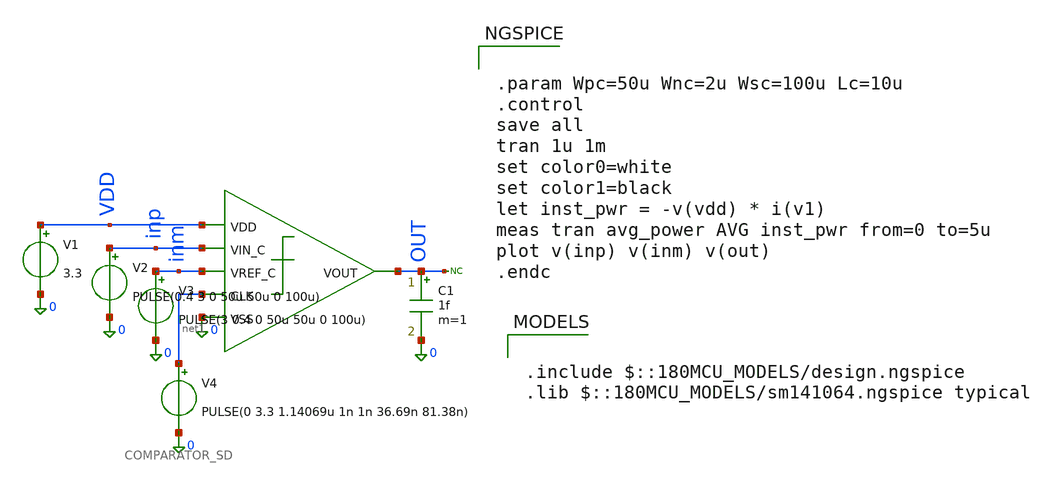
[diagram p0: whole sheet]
** sch_path: src/schematics/latched_comparator/COMP_TB.sch
**.subckt COMP_TB
* noconn OUT
V2 inp 0 PULSE(0.4 3 0 50u 50u 0 100u)
V4 net1 0 PULSE(0 3.3 1.14069u 1n 1n 36.69n 81.38n)
V1 VDD 0 3.3
C1 OUT 0 1f m=1
x1 VDD inp inm net1 OUT 0 COMPARATOR_SD
V3 inm 0 PULSE(3 0.4 0 50u 50u 0 100u)
**** begin user architecture code


.param Wpc=50u Wnc=2u Wsc=100u Lc=10u
.control
save all
tran 1u 1m
set color0=white
set color1=black
let inst_pwr = -v(vdd) * i(v1)
meas tran avg_power AVG inst_pwr from=0 to=5u
plot v(inp) v(inm) v(out)
.endc




.include $::180MCU_MODELS/design.ngspice
.lib $::180MCU_MODELS/sm141064.ngspice typical

**** end user architecture code
**.ends

* expanding   symbol:
*+  /foss/designs/low-power-12b-first-order-delta-sigma-adc/src/schematics/latched_comparator/COMPARATOR_SD.sym # of pins=6
** sym_path: /foss/designs/low-power-12b-first-order-delta-sigma-adc/src/schematics/latched_comparator/COMPARATOR_SD.sym
** sch_path: /foss/designs/low-power-12b-first-order-delta-sigma-adc/src/schematics/latched_comparator/COMPARATOR_SD.sch
.subckt COMPARATOR_SD VDD VIN_C VREF_C CLK VOUT VSS
*.ipin VIN_C
*.ipin VREF_C
*.ipin CLK
*.opin VOUT
*.ipin VDD
*.ipin VSS
XM1 net3 VIN_C net1 VDD pfet_03v3 L=Lc W=Wpc nf=1 ad='int((nf+1)/2) * W/nf * 0.18u' as='int((nf+2)/2) * W/nf * 0.18u'
+ pd='2*int((nf+1)/2) * (W/nf + 0.18u)' ps='2*int((nf+2)/2) * (W/nf + 0.18u)' nrd='0.18u / W' nrs='0.18u / W'
+ sa=0 sb=0 sd=0 m=1
XM2 net5 VREF_C net1 VDD pfet_03v3 L=Lc W=Wpc nf=1 ad='int((nf+1)/2) * W/nf * 0.18u' as='int((nf+2)/2) * W/nf * 0.18u'
+ pd='2*int((nf+1)/2) * (W/nf + 0.18u)' ps='2*int((nf+2)/2) * (W/nf + 0.18u)' nrd='0.18u / W' nrs='0.18u / W'
+ sa=0 sb=0 sd=0 m=1
XM3 VOUT net2 net5 VDD pfet_03v3 L=Lc W=Wpc nf=1 ad='int((nf+1)/2) * W/nf * 0.18u' as='int((nf+2)/2) * W/nf * 0.18u'
+ pd='2*int((nf+1)/2) * (W/nf + 0.18u)' ps='2*int((nf+2)/2) * (W/nf + 0.18u)' nrd='0.18u / W' nrs='0.18u / W'
+ sa=0 sb=0 sd=0 m=1
XM4 net4 net2 net3 VDD pfet_03v3 L=Lc W=Wpc nf=1 ad='int((nf+1)/2) * W/nf * 0.18u' as='int((nf+2)/2) * W/nf * 0.18u'
+ pd='2*int((nf+1)/2) * (W/nf + 0.18u)' ps='2*int((nf+2)/2) * (W/nf + 0.18u)' nrd='0.18u / W' nrs='0.18u / W'
+ sa=0 sb=0 sd=0 m=1
XM6 net2 CLK VDD VDD pfet_03v3 L=Lc W=Wpc nf=1 ad='int((nf+1)/2) * W/nf * 0.18u' as='int((nf+2)/2) * W/nf * 0.18u'
+ pd='2*int((nf+1)/2) * (W/nf + 0.18u)' ps='2*int((nf+2)/2) * (W/nf + 0.18u)' nrd='0.18u / W' nrs='0.18u / W'
+ sa=0 sb=0 sd=0 m=1
XM7 net2 CLK VSS VSS nfet_03v3 L=Lc W=Wnc nf=1 ad='int((nf+1)/2) * W/nf * 0.18u' as='int((nf+2)/2) * W/nf * 0.18u'
+ pd='2*int((nf+1)/2) * (W/nf + 0.18u)' ps='2*int((nf+2)/2) * (W/nf + 0.18u)' nrd='0.18u / W' nrs='0.18u / W'
+ sa=0 sb=0 sd=0 m=1
XM8 net4 CLK VOUT VSS nfet_03v3 L=Lc W=Wnc nf=1 ad='int((nf+1)/2) * W/nf * 0.18u' as='int((nf+2)/2) * W/nf * 0.18u'
+ pd='2*int((nf+1)/2) * (W/nf + 0.18u)' ps='2*int((nf+2)/2) * (W/nf + 0.18u)' nrd='0.18u / W' nrs='0.18u / W'
+ sa=0 sb=0 sd=0 m=1
XM9 net7 VOUT VDD VDD pfet_03v3 L=Lc W=Wpc nf=1 ad='int((nf+1)/2) * W/nf * 0.18u' as='int((nf+2)/2) * W/nf * 0.18u'
+ pd='2*int((nf+1)/2) * (W/nf + 0.18u)' ps='2*int((nf+2)/2) * (W/nf + 0.18u)' nrd='0.18u / W' nrs='0.18u / W'
+ sa=0 sb=0 sd=0 m=1
XM10 net4 CLK net7 VDD pfet_03v3 L=Lc W=Wpc nf=1 ad='int((nf+1)/2) * W/nf * 0.18u' as='int((nf+2)/2) * W/nf * 0.18u'
+ pd='2*int((nf+1)/2) * (W/nf + 0.18u)' ps='2*int((nf+2)/2) * (W/nf + 0.18u)' nrd='0.18u / W' nrs='0.18u / W'
+ sa=0 sb=0 sd=0 m=1
XM11 net4 VOUT VSS VSS nfet_03v3 L=Lc W=Wnc nf=1 ad='int((nf+1)/2) * W/nf * 0.18u' as='int((nf+2)/2) * W/nf * 0.18u'
+ pd='2*int((nf+1)/2) * (W/nf + 0.18u)' ps='2*int((nf+2)/2) * (W/nf + 0.18u)' nrd='0.18u / W' nrs='0.18u / W'
+ sa=0 sb=0 sd=0 m=1
XM12 net6 net4 VDD VDD pfet_03v3 L=Lc W=Wpc nf=1 ad='int((nf+1)/2) * W/nf * 0.18u' as='int((nf+2)/2) * W/nf * 0.18u'
+ pd='2*int((nf+1)/2) * (W/nf + 0.18u)' ps='2*int((nf+2)/2) * (W/nf + 0.18u)' nrd='0.18u / W' nrs='0.18u / W'
+ sa=0 sb=0 sd=0 m=1
XM13 VOUT CLK net6 VDD pfet_03v3 L=Lc W=Wpc nf=1 ad='int((nf+1)/2) * W/nf * 0.18u' as='int((nf+2)/2) * W/nf * 0.18u'
+ pd='2*int((nf+1)/2) * (W/nf + 0.18u)' ps='2*int((nf+2)/2) * (W/nf + 0.18u)' nrd='0.18u / W' nrs='0.18u / W'
+ sa=0 sb=0 sd=0 m=1
XM14 VOUT net4 VSS VSS nfet_03v3 L=Lc W=Wnc nf=1 ad='int((nf+1)/2) * W/nf * 0.18u' as='int((nf+2)/2) * W/nf * 0.18u'
+ pd='2*int((nf+1)/2) * (W/nf + 0.18u)' ps='2*int((nf+2)/2) * (W/nf + 0.18u)' nrd='0.18u / W' nrs='0.18u / W'
+ sa=0 sb=0 sd=0 m=1
XM5 net1 VSS VDD VDD pfet_03v3 L=Lc W=Wsc nf=1 ad='int((nf+1)/2) * W/nf * 0.18u' as='int((nf+2)/2) * W/nf * 0.18u'
+ pd='2*int((nf+1)/2) * (W/nf + 0.18u)' ps='2*int((nf+2)/2) * (W/nf + 0.18u)' nrd='0.18u / W' nrs='0.18u / W'
+ sa=0 sb=0 sd=0 m=1
.ends

.end
